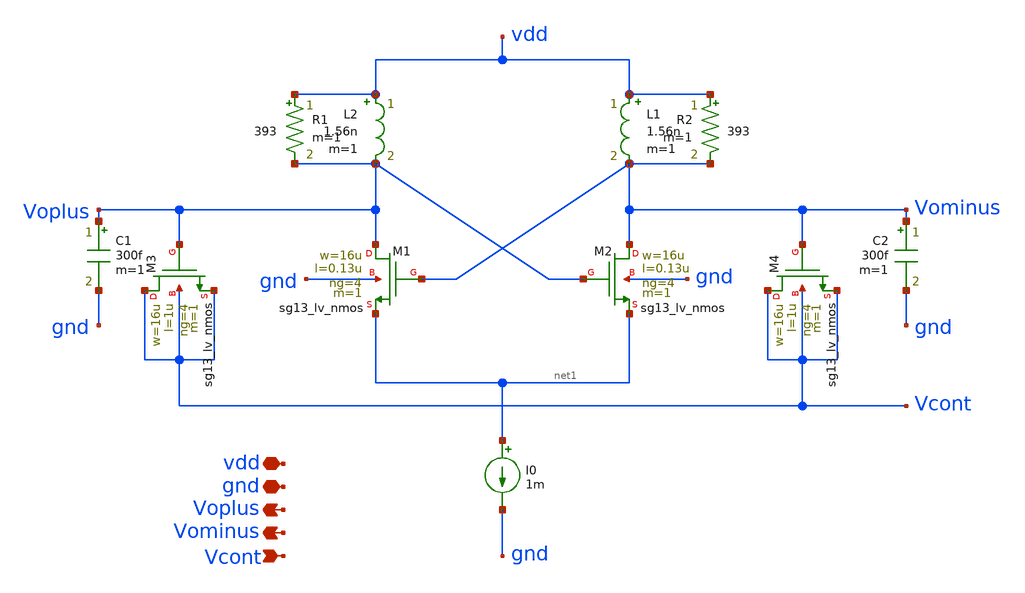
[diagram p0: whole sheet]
** sch_path: modules/module_4_type_2_PLL/LC_Oscillator/xschem/LC_Oscillator.sch
**.subckt LC_Oscillator vdd gnd Voplus Vominus Vcont
*.iopin vdd
*.iopin gnd
*.opin Voplus
*.opin Vominus
*.ipin Vcont
XM1 Voplus Vominus net1 gnd sg13_lv_nmos w=16u l=0.13u ng=4 m=1 mm_ok=1
XM2 Vominus Voplus net1 gnd sg13_lv_nmos w=16u l=0.13u ng=4 m=1 mm_ok=1
R2 vdd Vominus 393 m=1
I0 net1 gnd 1m
L1 vdd Vominus 1.56n m=1
R1 vdd Voplus 393 m=1
L2 vdd Voplus 1.56n m=1
C1 Voplus gnd 300f m=1
C2 Vominus gnd 300f m=1
XM3 Vcont Voplus Vcont Vcont sg13_lv_nmos w=16u l=1u ng=4 m=1 mm_ok=1
XM4 Vcont Vominus Vcont Vcont sg13_lv_nmos w=16u l=1u ng=4 m=1 mm_ok=1
**.ends
.end
